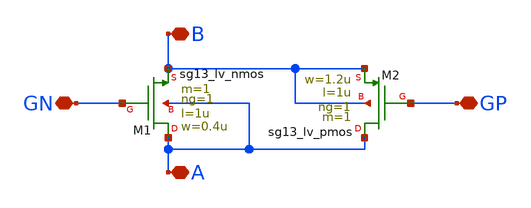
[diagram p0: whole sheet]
** sch_path: Python_layout/transmission_gate/transmission_gate.sch
**.subckt transmission_gate B GN A GP
*.iopin B
*.iopin GN
*.iopin A
*.iopin GP
XM1 A GN B A sg13_lv_nmos w=0.4u l=1u ng=1 m=1 mm_ok=1
XM2 A GP B B sg13_lv_pmos w=1.2u l=1u ng=1 m=1 mm_ok=1
**.ends
.end
